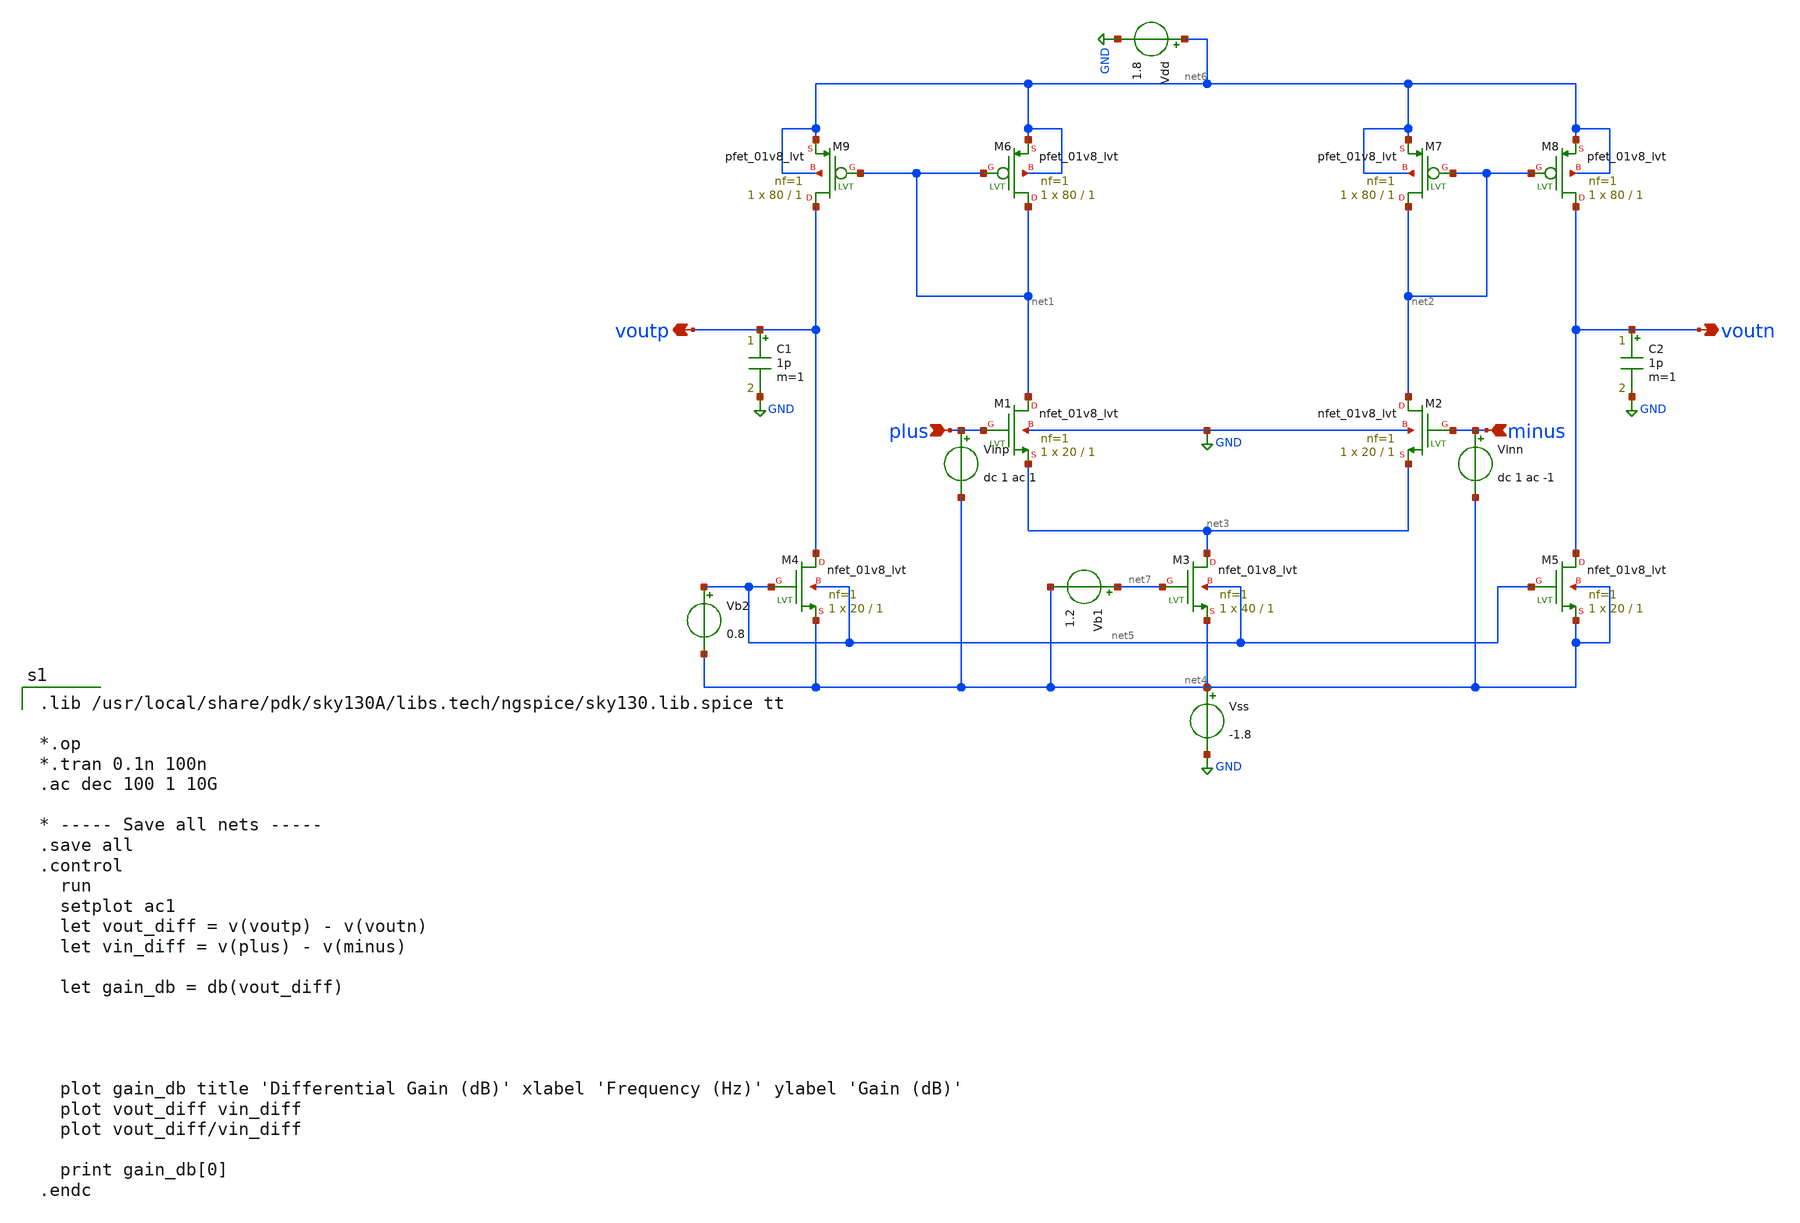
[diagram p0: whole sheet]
** sch_path: Final_project.sch
**.subckt Final_project minus plus voutn voutp
*.ipin minus
*.ipin plus
*.opin voutn
*.opin voutp
XM1 net1 plus net3 GND sky130_fd_pr__nfet_01v8_lvt L=1 W=20 nf=1 ad='int((1 + 1)/2) * 20 / 1 * 0.29'
+ as='int((1 + 2)/2) * 20 / 1 * 0.29' pd='2*int((1 + 1)/2) * (20 / 1 + 0.29)' ps='2*int((1 + 2)/2) * (20 / 1 + 0.29)'
+ nrd='0.29 / 20 ' nrs='0.29 / 20 ' sa=0 sb=0 sd=0 mult=1 m=1
XM2 net2 minus net3 GND sky130_fd_pr__nfet_01v8_lvt L=1 W=20 nf=1 ad='int((1 + 1)/2) * 20 / 1 * 0.29'
+ as='int((1 + 2)/2) * 20 / 1 * 0.29' pd='2*int((1 + 1)/2) * (20 / 1 + 0.29)' ps='2*int((1 + 2)/2) * (20 / 1 + 0.29)'
+ nrd='0.29 / 20 ' nrs='0.29 / 20 ' sa=0 sb=0 sd=0 mult=1 m=1
XM3 net3 net7 net4 net5 sky130_fd_pr__nfet_01v8_lvt L=1 W=40 nf=1 ad='int((1 + 1)/2) * 40 / 1 * 0.29'
+ as='int((1 + 2)/2) * 40 / 1 * 0.29' pd='2*int((1 + 1)/2) * (40 / 1 + 0.29)' ps='2*int((1 + 2)/2) * (40 / 1 + 0.29)'
+ nrd='0.29 / 40 ' nrs='0.29 / 40 ' sa=0 sb=0 sd=0 mult=1 m=1
XM4 voutp net5 net4 net5 sky130_fd_pr__nfet_01v8_lvt L=1 W=20 nf=1 ad='int((1 + 1)/2) * 20 / 1 * 0.29'
+ as='int((1 + 2)/2) * 20 / 1 * 0.29' pd='2*int((1 + 1)/2) * (20 / 1 + 0.29)' ps='2*int((1 + 2)/2) * (20 / 1 + 0.29)'
+ nrd='0.29 / 20 ' nrs='0.29 / 20 ' sa=0 sb=0 sd=0 mult=1 m=1
XM5 voutn net5 net4 net4 sky130_fd_pr__nfet_01v8_lvt L=1 W=20 nf=1 ad='int((1 + 1)/2) * 20 / 1 * 0.29'
+ as='int((1 + 2)/2) * 20 / 1 * 0.29' pd='2*int((1 + 1)/2) * (20 / 1 + 0.29)' ps='2*int((1 + 2)/2) * (20 / 1 + 0.29)'
+ nrd='0.29 / 20 ' nrs='0.29 / 20 ' sa=0 sb=0 sd=0 mult=1 m=1
XM6 net1 net1 net6 net6 sky130_fd_pr__pfet_01v8_lvt L=1 W=80 nf=1 ad='int((1 + 1)/2) * 80 / 1 * 0.29'
+ as='int((1 + 2)/2) * 80 / 1 * 0.29' pd='2*int((1 + 1)/2) * (80 / 1 + 0.29)' ps='2*int((1 + 2)/2) * (80 / 1 + 0.29)'
+ nrd='0.29 / 80 ' nrs='0.29 / 80 ' sa=0 sb=0 sd=0 mult=1 m=1
XM7 net2 net2 net6 net6 sky130_fd_pr__pfet_01v8_lvt L=1 W=80 nf=1 ad='int((1 + 1)/2) * 80 / 1 * 0.29'
+ as='int((1 + 2)/2) * 80 / 1 * 0.29' pd='2*int((1 + 1)/2) * (80 / 1 + 0.29)' ps='2*int((1 + 2)/2) * (80 / 1 + 0.29)'
+ nrd='0.29 / 80 ' nrs='0.29 / 80 ' sa=0 sb=0 sd=0 mult=1 m=1
XM8 voutn net2 net6 net6 sky130_fd_pr__pfet_01v8_lvt L=1 W=80 nf=1 ad='int((1 + 1)/2) * 80 / 1 * 0.29'
+ as='int((1 + 2)/2) * 80 / 1 * 0.29' pd='2*int((1 + 1)/2) * (80 / 1 + 0.29)' ps='2*int((1 + 2)/2) * (80 / 1 + 0.29)'
+ nrd='0.29 / 80 ' nrs='0.29 / 80 ' sa=0 sb=0 sd=0 mult=1 m=1
XM9 voutp net1 net6 net6 sky130_fd_pr__pfet_01v8_lvt L=1 W=80 nf=1 ad='int((1 + 1)/2) * 80 / 1 * 0.29'
+ as='int((1 + 2)/2) * 80 / 1 * 0.29' pd='2*int((1 + 1)/2) * (80 / 1 + 0.29)' ps='2*int((1 + 2)/2) * (80 / 1 + 0.29)'
+ nrd='0.29 / 80 ' nrs='0.29 / 80 ' sa=0 sb=0 sd=0 mult=1 m=1
Vdd net6 GND 1.8
Vss net4 GND -1.8
Vb2 net5 net4 0.8
Vb1 net7 net4 1.2
C1 voutp GND 1p m=1
C2 voutn GND 1p m=1
Vinp plus net4 dc 1 ac 1
Vinn minus net4 dc 1 ac -1
**** begin user architecture code

.lib /usr/local/share/pdk/sky130A/libs.tech/ngspice/sky130.lib.spice tt

*.op
*.tran 0.1n 100n
.ac dec 100 1 10G

* ----- Save all nets -----
.save all
.control
  run
  setplot ac1
  let vout_diff = v(voutp) - v(voutn)
  let vin_diff = v(plus) - v(minus)

  let gain_db = db(vout_diff)




  plot gain_db title 'Differential Gain (dB)' xlabel 'Frequency (Hz)' ylabel 'Gain (dB)'
  plot vout_diff vin_diff
  plot vout_diff/vin_diff

  print gain_db[0]
.endc

**** end user architecture code
**.ends
.GLOBAL GND
.end
